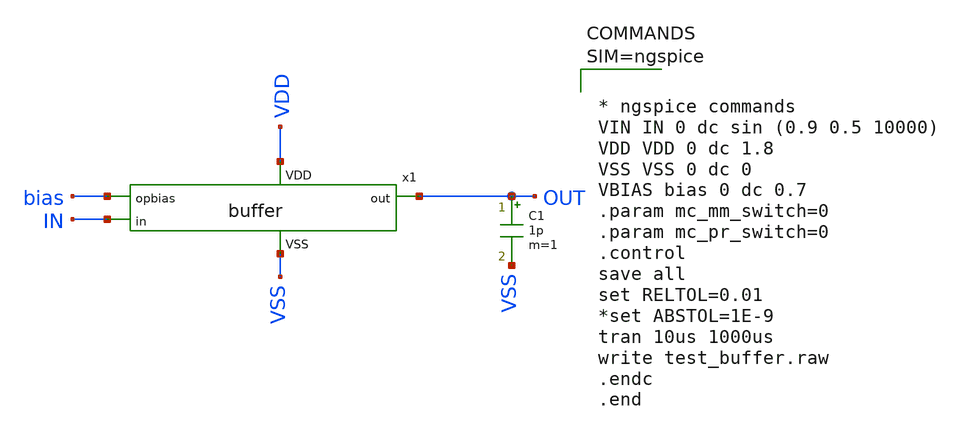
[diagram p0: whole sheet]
** sch_path: xschem/test_buffer.sch
**.subckt test_buffer
C1 OUT VSS 1p m=1
x1 bias IN OUT VSS VDD buffer
**** begin user architecture code

** opencircuitdesign pdks install
.lib $::SKYWATER_MODELS/sky130.lib.spice tt





* ngspice commands
VIN IN 0 dc sin (0.9 0.5 10000)
VDD VDD 0 dc 1.8
VSS VSS 0 dc 0
VBIAS bias 0 dc 0.7
.param mc_mm_switch=0
.param mc_pr_switch=0
.control
save all
set RELTOL=0.01
*set ABSTOL=1E-9
tran 10us 1000us
write test_buffer.raw
.endc
.end


**** end user architecture code
**.ends

* expanding   symbol:  buffer/buffer.sym # of pins=5
** sym_path: xschem/buffer/buffer.sym
** sch_path: xschem/buffer/buffer.sch
.subckt buffer opbias in out VSS VDD
*.ipin in
*.ipin opbias
*.opin out
*.iopin VSS
*.iopin VDD
x1 opbias in out out VSS VDD opamp
.ends


* expanding   symbol:  opamp/opamp.sym # of pins=6
** sym_path: xschem/opamp/opamp.sym
** sch_path: xschem/opamp/opamp.sch
.subckt opamp opbias inp inn out VSS VDD
*.ipin inp
*.ipin inn
*.ipin opbias
*.opin out
*.iopin VDD
*.iopin VSS
XC1 net5 out sky130_fd_pr__cap_mim_m3_1 W=2 L=4 MF=1 m=1
XC2 out net4 sky130_fd_pr__cap_mim_m3_1 W=2 L=4 MF=1 m=1
XM26 net2 opbias VDD VDD sky130_fd_pr__pfet_01v8_lvt L=3 W=10 nf=4 ad='int((4 + 1)/2) * 10 / 4 * 0.29'
+ as='int((4 + 2)/2) * 10 / 4 * 0.29' pd='2*int((4 + 1)/2) * (10 / 4 + 0.29)' ps='2*int((4 + 2)/2) * (10 / 4 + 0.29)'
+ nrd='0.29 / 10 ' nrs='0.29 / 10 ' sa=0 sb=0 sd=0 mult=1 m=1
XM3 net1 net1 VDD VDD sky130_fd_pr__pfet_01v8_lvt L=3 W=10 nf=2 ad='int((2 + 1)/2) * 10 / 2 * 0.29' as='int((2 + 2)/2) * 10 / 2 * 0.29'
+ pd='2*int((2 + 1)/2) * (10 / 2 + 0.29)' ps='2*int((2 + 2)/2) * (10 / 2 + 0.29)' nrd='0.29 / 10 ' nrs='0.29 / 10 '
+ sa=0 sb=0 sd=0 mult=1 m=1
XM4 net5 net1 VDD VDD sky130_fd_pr__pfet_01v8_lvt L=3 W=10 nf=2 ad='int((2 + 1)/2) * 10 / 2 * 0.29' as='int((2 + 2)/2) * 10 / 2 * 0.29'
+ pd='2*int((2 + 1)/2) * (10 / 2 + 0.29)' ps='2*int((2 + 2)/2) * (10 / 2 + 0.29)' nrd='0.29 / 10 ' nrs='0.29 / 10 '
+ sa=0 sb=0 sd=0 mult=1 m=1
XM10 out net5 VDD VDD sky130_fd_pr__pfet_01v8_lvt L=3 W=100 nf=5 ad='int((5 + 1)/2) * 100 / 5 * 0.29'
+ as='int((5 + 2)/2) * 100 / 5 * 0.29' pd='2*int((5 + 1)/2) * (100 / 5 + 0.29)' ps='2*int((5 + 2)/2) * (100 / 5 + 0.29)'
+ nrd='0.29 / 100 ' nrs='0.29 / 100 ' sa=0 sb=0 sd=0 mult=1 m=1
XM17 out net4 VSS VSS sky130_fd_pr__nfet_01v8_lvt L=3 W=80 nf=5 ad='int((5 + 1)/2) * 80 / 5 * 0.29' as='int((5 + 2)/2) * 80 / 5 * 0.29'
+ pd='2*int((5 + 1)/2) * (80 / 5 + 0.29)' ps='2*int((5 + 2)/2) * (80 / 5 + 0.29)' nrd='0.29 / 80 ' nrs='0.29 / 80 '
+ sa=0 sb=0 sd=0 mult=1 m=1
XM19 net4 net3 VSS VSS sky130_fd_pr__nfet_01v8_lvt L=3 W=5 nf=1 ad='int((1 + 1)/2) * 5 / 1 * 0.29' as='int((1 + 2)/2) * 5 / 1 * 0.29'
+ pd='2*int((1 + 1)/2) * (5 / 1 + 0.29)' ps='2*int((1 + 2)/2) * (5 / 1 + 0.29)' nrd='0.29 / 5 ' nrs='0.29 / 5 '
+ sa=0 sb=0 sd=0 mult=1 m=1
XM20 net3 net3 VSS VSS sky130_fd_pr__nfet_01v8_lvt L=3 W=5 nf=1 ad='int((1 + 1)/2) * 5 / 1 * 0.29' as='int((1 + 2)/2) * 5 / 1 * 0.29'
+ pd='2*int((1 + 1)/2) * (5 / 1 + 0.29)' ps='2*int((1 + 2)/2) * (5 / 1 + 0.29)' nrd='0.29 / 5 ' nrs='0.29 / 5 '
+ sa=0 sb=0 sd=0 mult=1 m=1
XM2 net1 net4 VSS VSS sky130_fd_pr__nfet_01v8_lvt L=3 W=8 nf=1 ad='int((1 + 1)/2) * 8 / 1 * 0.29' as='int((1 + 2)/2) * 8 / 1 * 0.29'
+ pd='2*int((1 + 1)/2) * (8 / 1 + 0.29)' ps='2*int((1 + 2)/2) * (8 / 1 + 0.29)' nrd='0.29 / 8 ' nrs='0.29 / 8 '
+ sa=0 sb=0 sd=0 mult=1 m=1
XM5 net5 net3 VSS VSS sky130_fd_pr__nfet_01v8_lvt L=3 W=8 nf=1 ad='int((1 + 1)/2) * 8 / 1 * 0.29' as='int((1 + 2)/2) * 8 / 1 * 0.29'
+ pd='2*int((1 + 1)/2) * (8 / 1 + 0.29)' ps='2*int((1 + 2)/2) * (8 / 1 + 0.29)' nrd='0.29 / 8 ' nrs='0.29 / 8 '
+ sa=0 sb=0 sd=0 mult=1 m=1
XM1 net3 inn net2 VDD sky130_fd_pr__pfet_01v8_lvt L=3 W=15 nf=3 ad='int((3 + 1)/2) * 15 / 3 * 0.29' as='int((3 + 2)/2) * 15 / 3 * 0.29'
+ pd='2*int((3 + 1)/2) * (15 / 3 + 0.29)' ps='2*int((3 + 2)/2) * (15 / 3 + 0.29)' nrd='0.29 / 15 ' nrs='0.29 / 15 '
+ sa=0 sb=0 sd=0 mult=1 m=1
XM6 net4 inp net2 VDD sky130_fd_pr__pfet_01v8_lvt L=3 W=15 nf=3 ad='int((3 + 1)/2) * 15 / 3 * 0.29' as='int((3 + 2)/2) * 15 / 3 * 0.29'
+ pd='2*int((3 + 1)/2) * (15 / 3 + 0.29)' ps='2*int((3 + 2)/2) * (15 / 3 + 0.29)' nrd='0.29 / 15 ' nrs='0.29 / 15 '
+ sa=0 sb=0 sd=0 mult=1 m=1
.ends

.end
